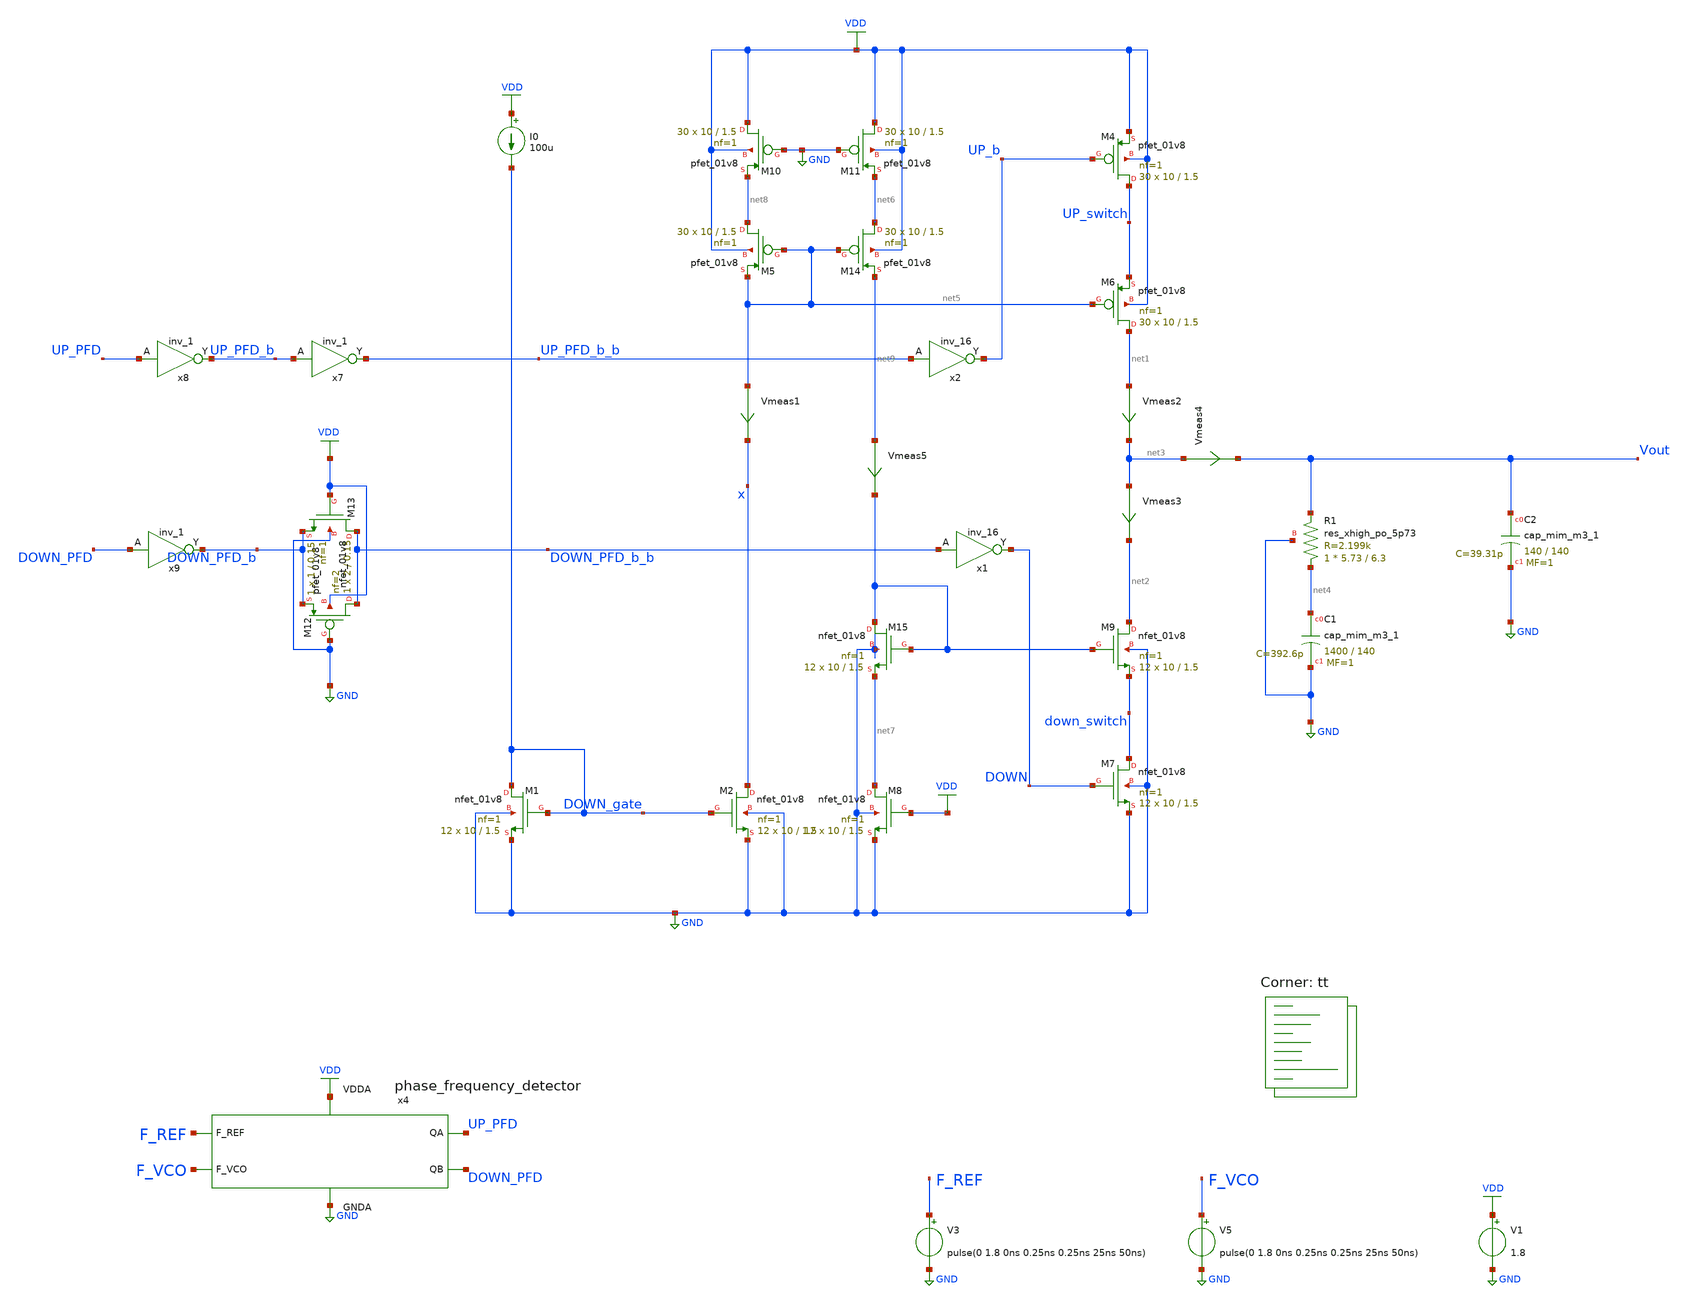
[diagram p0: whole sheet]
** sch_path: projects/pll/charge_pump/xschem_ngspice/pfd_charge_pump_3.sch
**.subckt pfd_charge_pump_3
XM1 DOWN_gate DOWN_gate GND GND sky130_fd_pr__nfet_01v8 L=1.5 W=10 nf=1 ad='int((nf+1)/2) * W/nf * 0.29'
+ as='int((nf+2)/2) * W/nf * 0.29' pd='2*int((nf+1)/2) * (W/nf + 0.29)' ps='2*int((nf+2)/2) * (W/nf + 0.29)'
+ nrd='0.29 / W' nrs='0.29 / W' sa=0 sb=0 sd=0 mult=12 m=12
XM2 x DOWN_gate GND GND sky130_fd_pr__nfet_01v8 L=1.5 W=10 nf=1 ad='int((nf+1)/2) * W/nf * 0.29' as='int((nf+2)/2) * W/nf * 0.29'
+ pd='2*int((nf+1)/2) * (W/nf + 0.29)' ps='2*int((nf+2)/2) * (W/nf + 0.29)' nrd='0.29 / W' nrs='0.29 / W'
+ sa=0 sb=0 sd=0 mult=12 m=12
V1 VDD GND 1.8
I0 VDD DOWN_gate 100u
Vmeas1 net5 x 0
.save i(vmeas1)
XM6 net1 net5 UP_switch VDD sky130_fd_pr__pfet_01v8 L=1.5 W=10 nf=1 ad='int((nf+1)/2) * W/nf * 0.29'
+ as='int((nf+2)/2) * W/nf * 0.29' pd='2*int((nf+1)/2) * (W/nf + 0.29)' ps='2*int((nf+2)/2) * (W/nf + 0.29)'
+ nrd='0.29 / W' nrs='0.29 / W' sa=0 sb=0 sd=0 mult=30 m=30
Vmeas2 net1 net3 0
.save i(vmeas2)
Vmeas3 net3 net2 0
.save i(vmeas3)
XM9 net2 GND down_switch GND sky130_fd_pr__nfet_01v8 L=1.5 W=10 nf=1 ad='int((nf+1)/2) * W/nf * 0.29'
+ as='int((nf+2)/2) * W/nf * 0.29' pd='2*int((nf+1)/2) * (W/nf + 0.29)' ps='2*int((nf+2)/2) * (W/nf + 0.29)'
+ nrd='0.29 / W' nrs='0.29 / W' sa=0 sb=0 sd=0 mult=12 m=12
XM12 DOWN_PFD_b_b GND DOWN_PFD_b VDD sky130_fd_pr__pfet_01v8 L=0.15 W=2 nf=2 ad='int((nf+1)/2) * W/nf * 0.29'
+ as='int((nf+2)/2) * W/nf * 0.29' pd='2*int((nf+1)/2) * (W/nf + 0.29)' ps='2*int((nf+2)/2) * (W/nf + 0.29)'
+ nrd='0.29 / W' nrs='0.29 / W' sa=0 sb=0 sd=0 mult=1 m=1
XM13 DOWN_PFD_b_b VDD DOWN_PFD_b GND sky130_fd_pr__nfet_01v8 L=0.15 W=1 nf=1 ad='int((nf+1)/2) * W/nf * 0.29'
+ as='int((nf+2)/2) * W/nf * 0.29' pd='2*int((nf+1)/2) * (W/nf + 0.29)' ps='2*int((nf+2)/2) * (W/nf + 0.29)'
+ nrd='0.29 / W' nrs='0.29 / W' sa=0 sb=0 sd=0 mult=1 m=1
x7 UP_PFD_b GND GND VDD VDD UP_PFD_b_b sky130_fd_sc_hd__inv_1
x8 UP_PFD GND GND VDD VDD UP_PFD_b sky130_fd_sc_hd__inv_1
x9 DOWN_PFD GND GND VDD VDD DOWN_PFD_b sky130_fd_sc_hd__inv_1
XC2 Vout GND sky130_fd_pr__cap_mim_m3_1 W=140 L=140 MF=1 m=1
XC1 net4 GND sky130_fd_pr__cap_mim_m3_1 W=1400 L=140 MF=1 m=1
V3 F_REF GND pulse(0 1.8 0ns 0.25ns 0.25ns 25ns 50ns)
V5 F_VCO GND pulse(0 1.8 0ns 0.25ns 0.25ns 25ns 50ns)
x4 F_REF F_VCO VDD UP_PFD DOWN_PFD GND phase_frequency_detector
XR1 net4 Vout GND sky130_fd_pr__res_xhigh_po_5p73 L=6.3 mult=1 m=1
Vmeas4 net3 Vout 0
.save i(vmeas4)
XM4 UP_switch UP_b VDD VDD sky130_fd_pr__pfet_01v8 L=1.5 W=10 nf=1 ad='int((nf+1)/2) * W/nf * 0.29' as='int((nf+2)/2) * W/nf * 0.29'
+ pd='2*int((nf+1)/2) * (W/nf + 0.29)' ps='2*int((nf+2)/2) * (W/nf + 0.29)' nrd='0.29 / W' nrs='0.29 / W'
+ sa=0 sb=0 sd=0 mult=30 m=30
XM5 net8 net5 net5 VDD sky130_fd_pr__pfet_01v8 L=1.5 W=10 nf=1 ad='int((nf+1)/2) * W/nf * 0.29' as='int((nf+2)/2) * W/nf * 0.29'
+ pd='2*int((nf+1)/2) * (W/nf + 0.29)' ps='2*int((nf+2)/2) * (W/nf + 0.29)' nrd='0.29 / W' nrs='0.29 / W'
+ sa=0 sb=0 sd=0 mult=30 m=30
XM10 VDD GND net8 VDD sky130_fd_pr__pfet_01v8 L=1.5 W=10 nf=1 ad='int((nf+1)/2) * W/nf * 0.29' as='int((nf+2)/2) * W/nf * 0.29'
+ pd='2*int((nf+1)/2) * (W/nf + 0.29)' ps='2*int((nf+2)/2) * (W/nf + 0.29)' nrd='0.29 / W' nrs='0.29 / W'
+ sa=0 sb=0 sd=0 mult=30 m=30
XM11 VDD GND net6 VDD sky130_fd_pr__pfet_01v8 L=1.5 W=10 nf=1 ad='int((nf+1)/2) * W/nf * 0.29' as='int((nf+2)/2) * W/nf * 0.29'
+ pd='2*int((nf+1)/2) * (W/nf + 0.29)' ps='2*int((nf+2)/2) * (W/nf + 0.29)' nrd='0.29 / W' nrs='0.29 / W'
+ sa=0 sb=0 sd=0 mult=30 m=30
XM14 net6 net5 net9 VDD sky130_fd_pr__pfet_01v8 L=1.5 W=10 nf=1 ad='int((nf+1)/2) * W/nf * 0.29' as='int((nf+2)/2) * W/nf * 0.29'
+ pd='2*int((nf+1)/2) * (W/nf + 0.29)' ps='2*int((nf+2)/2) * (W/nf + 0.29)' nrd='0.29 / W' nrs='0.29 / W'
+ sa=0 sb=0 sd=0 mult=30 m=30
XM7 down_switch DOWN GND GND sky130_fd_pr__nfet_01v8 L=1.5 W=10 nf=1 ad='int((nf+1)/2) * W/nf * 0.29'
+ as='int((nf+2)/2) * W/nf * 0.29' pd='2*int((nf+1)/2) * (W/nf + 0.29)' ps='2*int((nf+2)/2) * (W/nf + 0.29)'
+ nrd='0.29 / W' nrs='0.29 / W' sa=0 sb=0 sd=0 mult=12 m=12
XM8 net7 VDD GND GND sky130_fd_pr__nfet_01v8 L=1.5 W=10 nf=1 ad='int((nf+1)/2) * W/nf * 0.29' as='int((nf+2)/2) * W/nf * 0.29'
+ pd='2*int((nf+1)/2) * (W/nf + 0.29)' ps='2*int((nf+2)/2) * (W/nf + 0.29)' nrd='0.29 / W' nrs='0.29 / W'
+ sa=0 sb=0 sd=0 mult=12 m=12
XM15 GND GND net7 GND sky130_fd_pr__nfet_01v8 L=1.5 W=10 nf=1 ad='int((nf+1)/2) * W/nf * 0.29' as='int((nf+2)/2) * W/nf * 0.29'
+ pd='2*int((nf+1)/2) * (W/nf + 0.29)' ps='2*int((nf+2)/2) * (W/nf + 0.29)' nrd='0.29 / W' nrs='0.29 / W'
+ sa=0 sb=0 sd=0 mult=12 m=12
Vmeas5 net9 GND 0
.save i(vmeas5)
x2 UP_PFD_b_b GND GND VDD VDD UP_b sky130_fd_sc_hd__inv_16
x1 DOWN_PFD_b_b GND GND VDD VDD DOWN sky130_fd_sc_hd__inv_16
**** begin user architecture code
.lib $::SKYWATER_MODELS/sky130.lib.spice tt



.include /foss/pdks/sky130A/libs.ref/sky130_fd_sc_hd/spice/sky130_fd_sc_hd.spice

.option method=gear trtol1
.option wnflag=1
* .option savecurrents

* .temp = 75

.ic v(vout) = 1.2

.save  v(up_pfd) v(down_pfd) v(up_pfd_b) v(up_pfd_b_b) v(down_pfd_b) v(down_pfd_b_b) v(up) v(up_b) v(down) v(down_b) v(v2) v(x) v(vout) v(up_switch) v(down_switch) v(x2.p_bias) v(x2.n_bias) v(x2.v_common_p) v(x2.v_common_n) v(x2.p_left) v(x2.p_right) v(x2.n_left) v(x2.n_right) v(f_ref) v(f_vco) v(x4.qa) v(x4.qa_b) v(x4.qb) v(x4.qb_b) v(x4.qa) v(x4.e) v(x4.e_b) v(x4.f) v(x4.f_b) v(x4.before_reset) v(x4.reset)


.control
  * save v(up_pfd) v(down_pfd) v(up_pfd_b) v(down_pfd_b) v(up) v(up_b) v(down) v(down_b) v(x)
+ v(vout) v(up_input) v(down_input)
  * save all

  tran 1ns 10us
  * dc v2 0 1.8 0.01
  remzerovec
  write pfd_charge_pump_3.raw
  * wrdata /foss/designs/my_design/projects/pll/pfd/xschem_ngspice/charge_pump2_QA.txt v(osc)
  set appendwrite

.endc






**** end user architecture code
**.ends

* expanding   symbol:
*+  /foss/designs/my_design/projects/pll/pfd/xschem_ngspice/phase_frequency_detector.sym # of pins=6
** sym_path: projects/pll/pfd/xschem_ngspice/phase_frequency_detector.sym
** sch_path: projects/pll/pfd/xschem_ngspice/phase_frequency_detector.sch
.subckt phase_frequency_detector F_REF F_VCO VDDA QA QB GNDA
*.ipin F_REF
*.opin QA
*.ipin F_VCO
*.opin QB
*.ipin VDDA
*.ipin GNDA
x1 F_REF QA GNDA GNDA VDDA VDDA QA_b sky130_fd_sc_hd__nor2_1
x2 QA_b E GNDA GNDA VDDA VDDA QA sky130_fd_sc_hd__nor2_1
x3 QA_b E_b GNDA GNDA VDDA VDDA E sky130_fd_sc_hd__nor2_1
x4 E Reset GNDA GNDA VDDA VDDA E_b sky130_fd_sc_hd__nor2_1
x5 F_VCO QB GNDA GNDA VDDA VDDA QB_b sky130_fd_sc_hd__nor2_1
x6 QB_b F GNDA GNDA VDDA VDDA QB sky130_fd_sc_hd__nor2_1
x7 QB_b F_b GNDA GNDA VDDA VDDA F sky130_fd_sc_hd__nor2_1
x8 F Reset GNDA GNDA VDDA VDDA F_b sky130_fd_sc_hd__nor2_1
x9 QA QB GNDA GNDA VDDA VDDA before_Reset sky130_fd_sc_hd__nand2_1
x10 before_Reset GNDA GNDA VDDA VDDA net1 sky130_fd_sc_hd__inv_1
x11 net1 GNDA GNDA VDDA VDDA net2 sky130_fd_sc_hd__inv_1
x12 net2 GNDA GNDA VDDA VDDA net3 sky130_fd_sc_hd__inv_1
x13 net3 GNDA GNDA VDDA VDDA net4 sky130_fd_sc_hd__inv_1
x14 net4 GNDA GNDA VDDA VDDA Reset sky130_fd_sc_hd__inv_1
.ends

.GLOBAL VDD
.GLOBAL GND
.end
